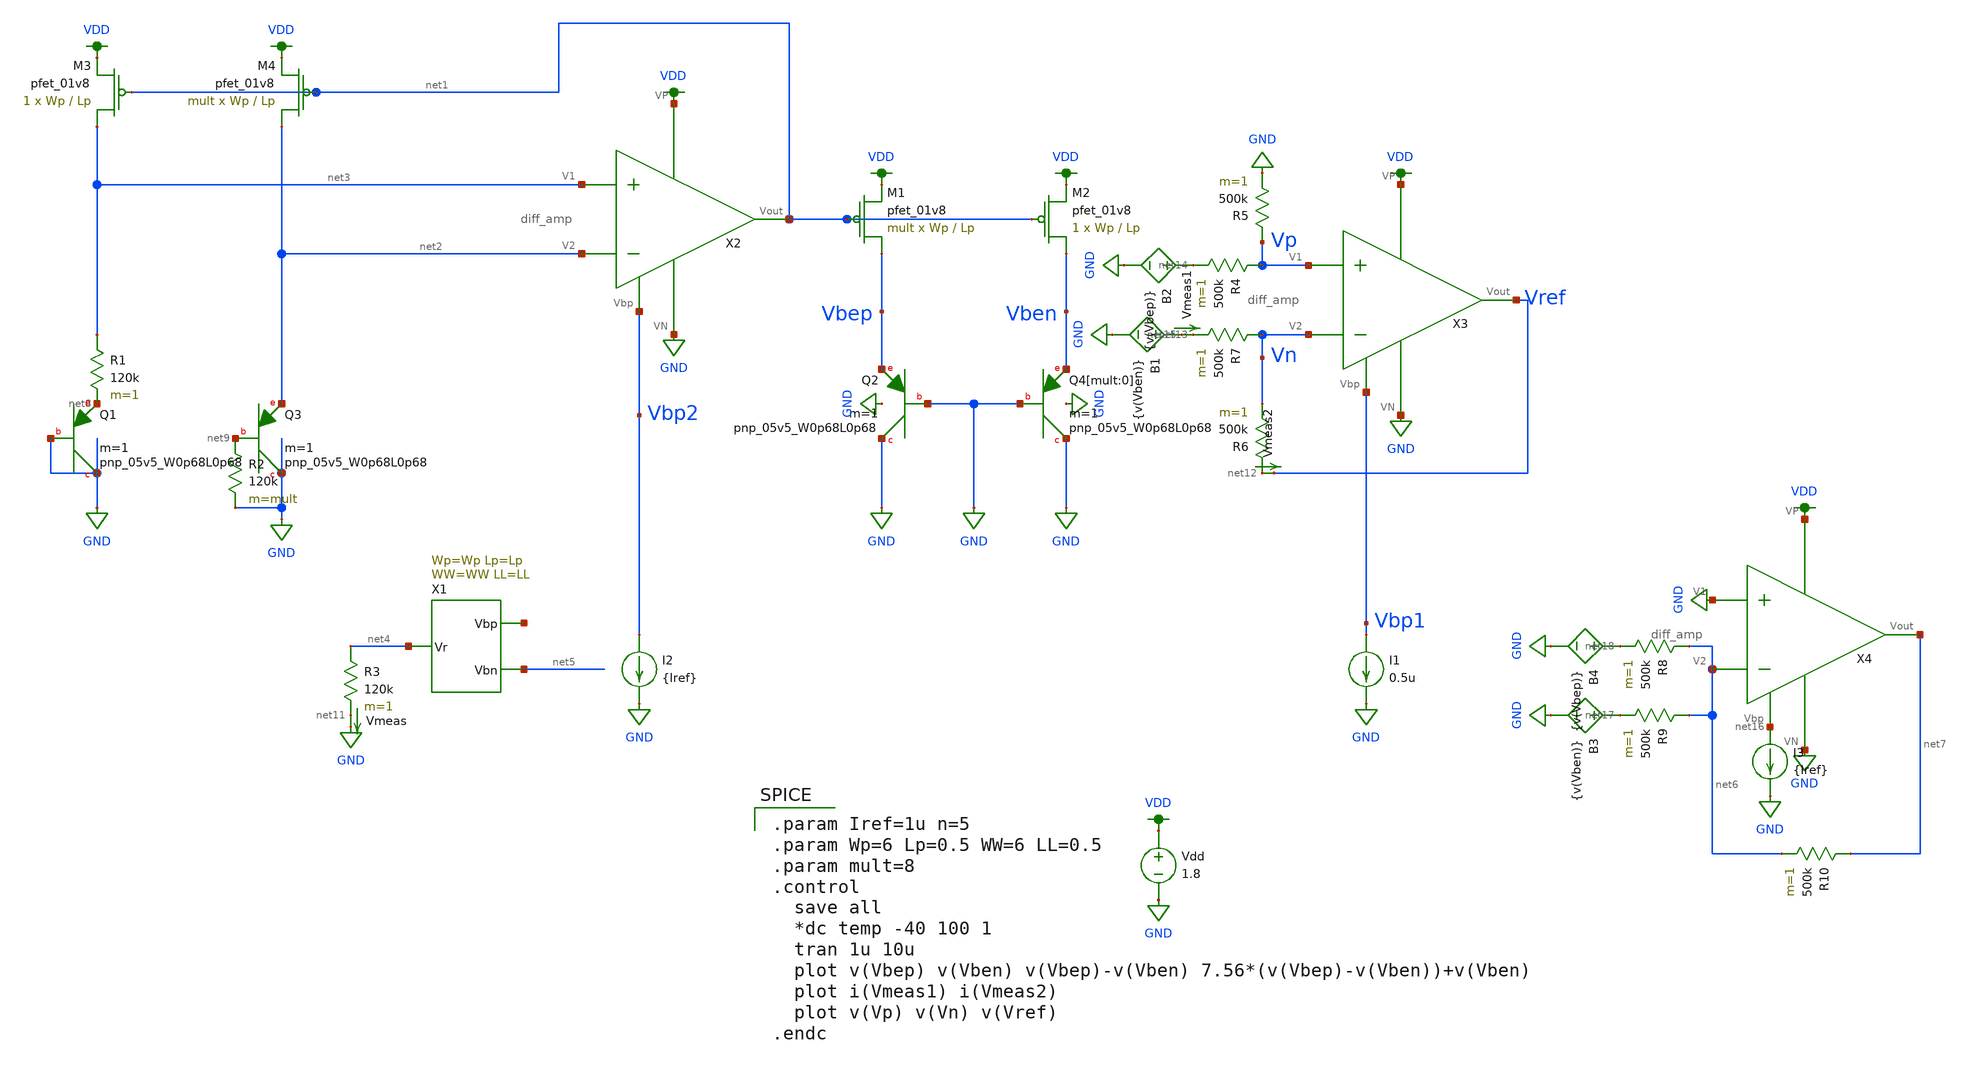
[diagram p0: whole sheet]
** sch_path: schematic/test/archive/bandgap_dctemp.sch
**.subckt bandgap_dctemp
XQ2 GND GND Vbep sky130_fd_pr__pnp_05v5_W0p68L0p68 m=1
Vdd VDD GND 1.8
XM1 Vbep net1 VDD VDD sky130_fd_pr__pfet_01v8 L=Lp W=Wp nf=1 ad='int((nf+1)/2) * W/nf * 0.29' as='int((nf+2)/2) * W/nf * 0.29'
+ pd='2*int((nf+1)/2) * (W/nf + 0.29)' ps='2*int((nf+2)/2) * (W/nf + 0.29)' nrd='0.29 / W' nrs='0.29 / W'
+ sa=0 sb=0 sd=0 mult=mult m=mult
XM2 Vben net1 VDD VDD sky130_fd_pr__pfet_01v8 L=Lp W=Wp nf=1 ad='int((nf+1)/2) * W/nf * 0.29' as='int((nf+2)/2) * W/nf * 0.29'
+ pd='2*int((nf+1)/2) * (W/nf + 0.29)' ps='2*int((nf+2)/2) * (W/nf + 0.29)' nrd='0.29 / W' nrs='0.29 / W'
+ sa=0 sb=0 sd=0 mult=1 m=1
XQ4[mult:0] GND GND Vben sky130_fd_pr__pnp_05v5_W0p68L0p68 m=1
XQ1 GND GND net8 sky130_fd_pr__pnp_05v5_W0p68L0p68 m=1
XQ3 GND net9 net2 sky130_fd_pr__pnp_05v5_W0p68L0p68 m=1
R1 net3 net8 120k m=1
R2 net9 GND 120k m=mult
XM3 net3 net1 VDD VDD sky130_fd_pr__pfet_01v8 L=Lp W=Wp nf=1 ad='int((nf+1)/2) * W/nf * 0.29' as='int((nf+2)/2) * W/nf * 0.29'
+ pd='2*int((nf+1)/2) * (W/nf + 0.29)' ps='2*int((nf+2)/2) * (W/nf + 0.29)' nrd='0.29 / W' nrs='0.29 / W'
+ sa=0 sb=0 sd=0 mult=1 m=1
XM4 net2 net1 VDD VDD sky130_fd_pr__pfet_01v8 L=Lp W=Wp nf=1 ad='int((nf+1)/2) * W/nf * 0.29' as='int((nf+2)/2) * W/nf * 0.29'
+ pd='2*int((nf+1)/2) * (W/nf + 0.29)' ps='2*int((nf+2)/2) * (W/nf + 0.29)' nrd='0.29 / W' nrs='0.29 / W'
+ sa=0 sb=0 sd=0 mult=mult m=mult
X1 net4 net5 net10 ibias Wp=Wp Lp=Lp WW=WW LL=LL
R3 net4 net11 120k m=1
Vmeas net11 GND 0
.save i(vmeas)
R6 net12 Vn 500k m=1
X3 VDD Vbp1 Vref Vp Vn GND diff_amp
X2 VDD Vbp2 net1 net3 net2 GND diff_amp
R7 Vn net13 500k m=1
R4 Vp net14 500k m=1
R5 Vp GND 500k m=1
Vmeas1 net15 net13 0
.save i(vmeas1)
Vmeas2 net12 Vref 0
.save i(vmeas2)
I1 Vbp1 GND 0.5u
I2 Vbp2 GND {Iref}
X4 VDD net16 net7 GND net6 GND diff_amp
I3 net16 GND {Iref}
B1 net15 GND V={v(Vben)}
B2 net14 GND V={v(Vbep)}
B3 net17 GND V={v(Vben)}
B4 net18 GND V={v(Vbep)}
R8 net6 net18 500k m=1
R9 net6 net17 500k m=1
R10 net7 net6 500k m=1
**** begin user architecture code

.option wnflag=1
.param MC_SWITCH=0.0
.lib /media/qdeng/526448C32060CF5C/skywater/skywater-pdk/libraries/sky130_fd_pr_ngspice/latest/models/sky130.lib.spice tt


.param Iref=1u n=5
.param Wp=6 Lp=0.5 WW=6 LL=0.5
.param mult=8
.control
  save all
  *dc temp -40 100 1
  tran 1u 10u
  plot v(Vbep) v(Vben) v(Vbep)-v(Vben) 7.56*(v(Vbep)-v(Vben))+v(Vben)
  plot i(Vmeas1) i(Vmeas2)
  plot v(Vp) v(Vn) v(Vref)
.endc

**** end user architecture code
**.ends
.GLOBAL GND
.GLOBAL VDD
.end
